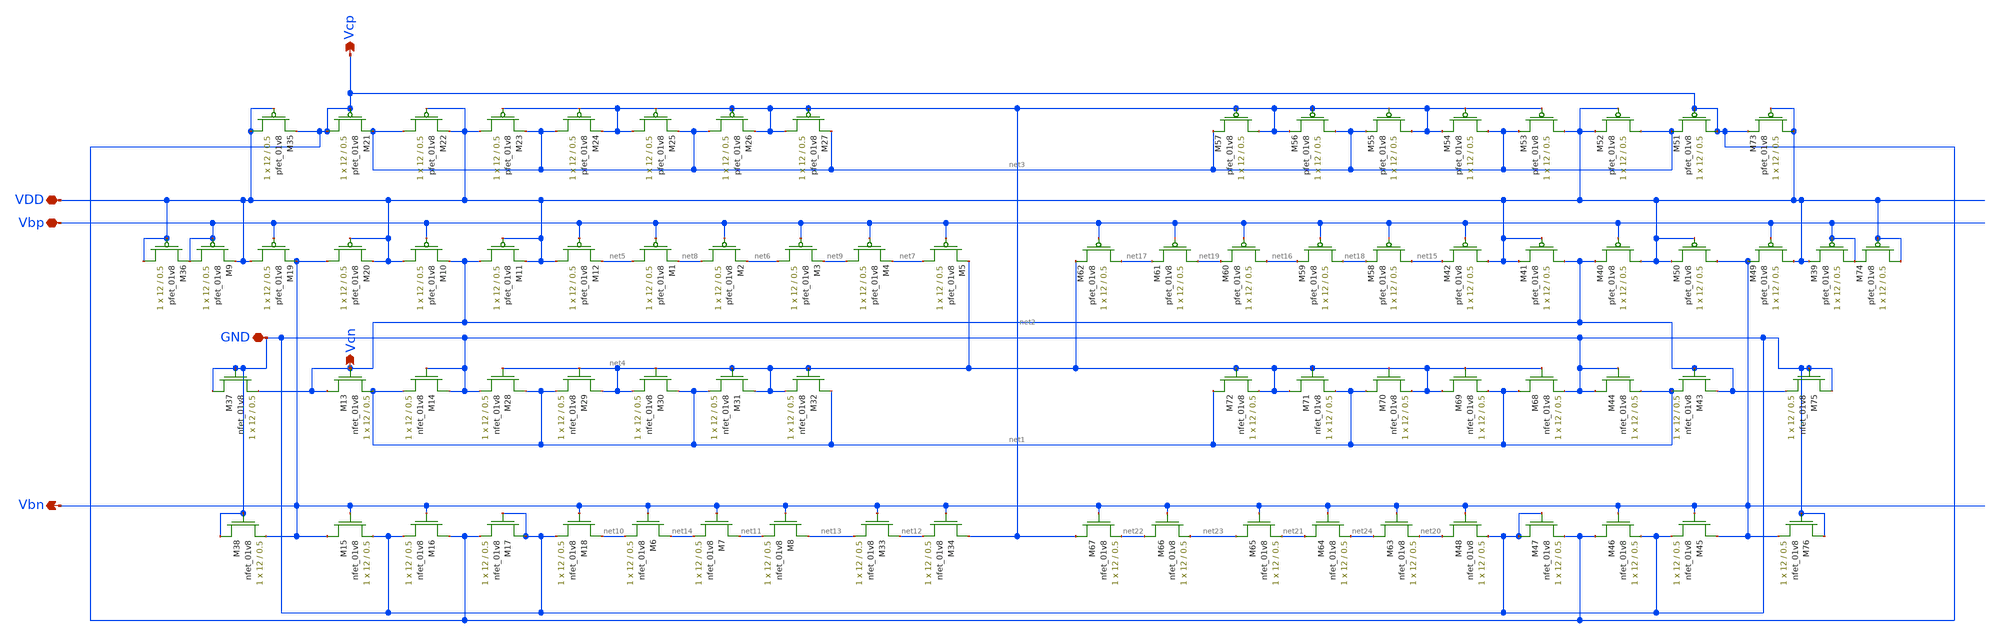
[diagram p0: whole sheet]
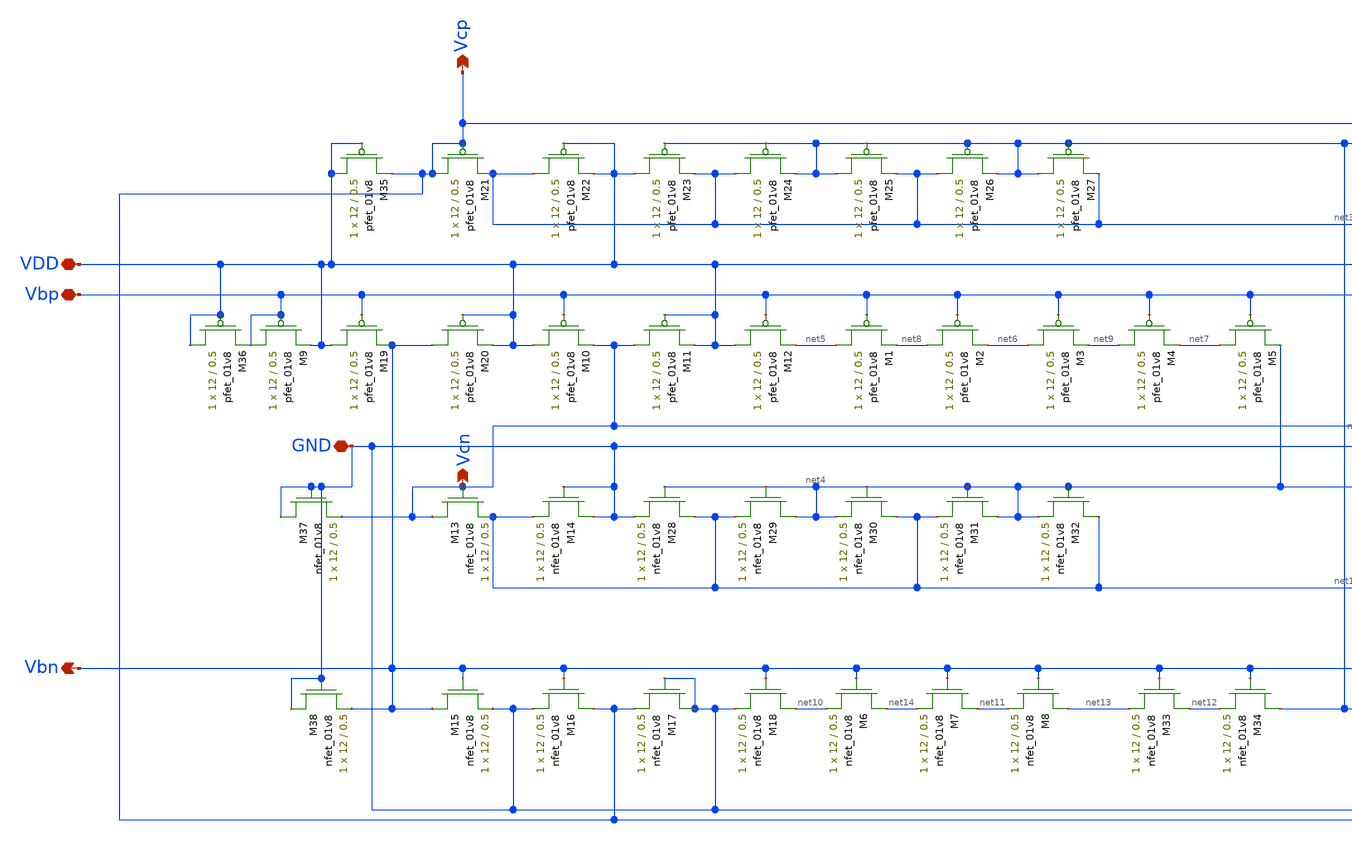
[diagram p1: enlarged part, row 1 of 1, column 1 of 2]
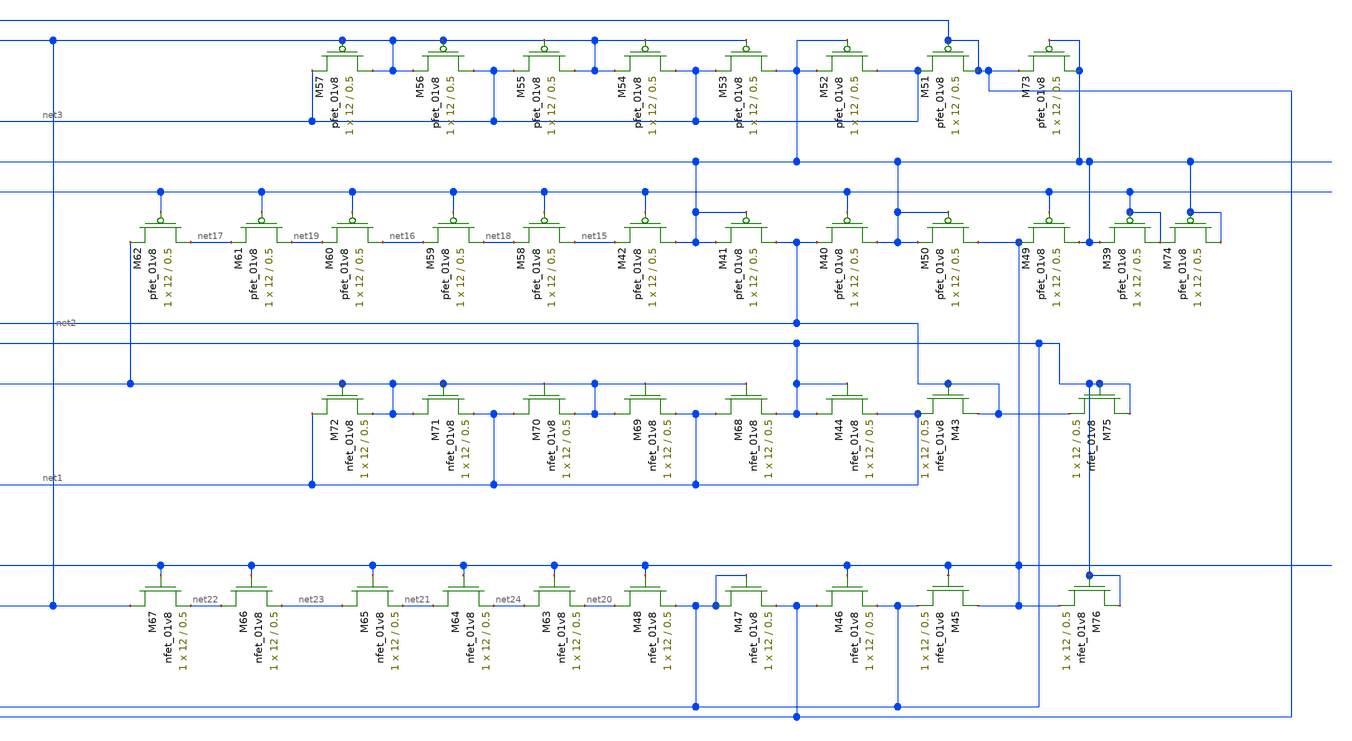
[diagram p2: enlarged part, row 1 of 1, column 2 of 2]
** sch_path: Miniproject3/Bias/LDS_Cascode_bias_voltage_generator.sch
**.subckt LDS_Cascode_bias_voltage_generator VDD Vbp Vcn GND Vbn Vcp
*.iopin VDD
*.iopin Vbp
*.opin Vcn
*.iopin GND
*.opin Vbn
*.opin Vcp
XM9 Vbp Vbp VDD VDD sky130_fd_pr__pfet_01v8 L=0.5 W=12 nf=1 ad='int((nf+1)/2) * W/nf * 0.29' as='int((nf+2)/2) * W/nf * 0.29'
+ pd='2*int((nf+1)/2) * (W/nf + 0.29)' ps='2*int((nf+2)/2) * (W/nf + 0.29)' nrd='0.29 / W' nrs='0.29 / W'
+ sa=0 sb=0 sd=0 mult=1 m=1
XM10 VDD Vbp Vcn VDD sky130_fd_pr__pfet_01v8 L=0.5 W=12 nf=1 ad='int((nf+1)/2) * W/nf * 0.29' as='int((nf+2)/2) * W/nf * 0.29'
+ pd='2*int((nf+1)/2) * (W/nf + 0.29)' ps='2*int((nf+2)/2) * (W/nf + 0.29)' nrd='0.29 / W' nrs='0.29 / W'
+ sa=0 sb=0 sd=0 mult=1 m=1
XM11 Vcn VDD VDD VDD sky130_fd_pr__pfet_01v8 L=0.5 W=12 nf=1 ad='int((nf+1)/2) * W/nf * 0.29' as='int((nf+2)/2) * W/nf * 0.29'
+ pd='2*int((nf+1)/2) * (W/nf + 0.29)' ps='2*int((nf+2)/2) * (W/nf + 0.29)' nrd='0.29 / W' nrs='0.29 / W'
+ sa=0 sb=0 sd=0 mult=1 m=1
XM12 VDD Vbp net5 VDD sky130_fd_pr__pfet_01v8 L=0.5 W=12 nf=1 ad='int((nf+1)/2) * W/nf * 0.29' as='int((nf+2)/2) * W/nf * 0.29'
+ pd='2*int((nf+1)/2) * (W/nf + 0.29)' ps='2*int((nf+2)/2) * (W/nf + 0.29)' nrd='0.29 / W' nrs='0.29 / W'
+ sa=0 sb=0 sd=0 mult=1 m=1
XM13 Vcn Vcn net1 GND sky130_fd_pr__nfet_01v8 L=0.5 W=12 nf=1 ad='int((nf+1)/2) * W/nf * 0.29' as='int((nf+2)/2) * W/nf * 0.29'
+ pd='2*int((nf+1)/2) * (W/nf + 0.29)' ps='2*int((nf+2)/2) * (W/nf + 0.29)' nrd='0.29 / W' nrs='0.29 / W'
+ sa=0 sb=0 sd=0 mult=1 m=1
XM14 GND GND net1 GND sky130_fd_pr__nfet_01v8 L=0.5 W=12 nf=1 ad='int((nf+1)/2) * W/nf * 0.29' as='int((nf+2)/2) * W/nf * 0.29'
+ pd='2*int((nf+1)/2) * (W/nf + 0.29)' ps='2*int((nf+2)/2) * (W/nf + 0.29)' nrd='0.29 / W' nrs='0.29 / W'
+ sa=0 sb=0 sd=0 mult=1 m=1
XM15 Vbn Vbn GND GND sky130_fd_pr__nfet_01v8 L=0.5 W=12 nf=1 ad='int((nf+1)/2) * W/nf * 0.29' as='int((nf+2)/2) * W/nf * 0.29'
+ pd='2*int((nf+1)/2) * (W/nf + 0.29)' ps='2*int((nf+2)/2) * (W/nf + 0.29)' nrd='0.29 / W' nrs='0.29 / W'
+ sa=0 sb=0 sd=0 mult=1 m=1
XM16 Vcp Vbn GND GND sky130_fd_pr__nfet_01v8 L=0.5 W=12 nf=1 ad='int((nf+1)/2) * W/nf * 0.29' as='int((nf+2)/2) * W/nf * 0.29'
+ pd='2*int((nf+1)/2) * (W/nf + 0.29)' ps='2*int((nf+2)/2) * (W/nf + 0.29)' nrd='0.29 / W' nrs='0.29 / W'
+ sa=0 sb=0 sd=0 mult=1 m=1
XM17 GND GND Vcp GND sky130_fd_pr__nfet_01v8 L=0.5 W=12 nf=1 ad='int((nf+1)/2) * W/nf * 0.29' as='int((nf+2)/2) * W/nf * 0.29'
+ pd='2*int((nf+1)/2) * (W/nf + 0.29)' ps='2*int((nf+2)/2) * (W/nf + 0.29)' nrd='0.29 / W' nrs='0.29 / W'
+ sa=0 sb=0 sd=0 mult=1 m=1
XM18 net10 Vbn GND GND sky130_fd_pr__nfet_01v8 L=0.5 W=12 nf=1 ad='int((nf+1)/2) * W/nf * 0.29' as='int((nf+2)/2) * W/nf * 0.29'
+ pd='2*int((nf+1)/2) * (W/nf + 0.29)' ps='2*int((nf+2)/2) * (W/nf + 0.29)' nrd='0.29 / W' nrs='0.29 / W'
+ sa=0 sb=0 sd=0 mult=1 m=1
XM19 VDD Vbp Vbn VDD sky130_fd_pr__pfet_01v8 L=0.5 W=12 nf=1 ad='int((nf+1)/2) * W/nf * 0.29' as='int((nf+2)/2) * W/nf * 0.29'
+ pd='2*int((nf+1)/2) * (W/nf + 0.29)' ps='2*int((nf+2)/2) * (W/nf + 0.29)' nrd='0.29 / W' nrs='0.29 / W'
+ sa=0 sb=0 sd=0 mult=1 m=1
XM20 Vbn VDD VDD VDD sky130_fd_pr__pfet_01v8 L=0.5 W=12 nf=1 ad='int((nf+1)/2) * W/nf * 0.29' as='int((nf+2)/2) * W/nf * 0.29'
+ pd='2*int((nf+1)/2) * (W/nf + 0.29)' ps='2*int((nf+2)/2) * (W/nf + 0.29)' nrd='0.29 / W' nrs='0.29 / W'
+ sa=0 sb=0 sd=0 mult=1 m=1
XM21 Vcp Vcp net3 VDD sky130_fd_pr__pfet_01v8 L=0.5 W=12 nf=1 ad='int((nf+1)/2) * W/nf * 0.29' as='int((nf+2)/2) * W/nf * 0.29'
+ pd='2*int((nf+1)/2) * (W/nf + 0.29)' ps='2*int((nf+2)/2) * (W/nf + 0.29)' nrd='0.29 / W' nrs='0.29 / W'
+ sa=0 sb=0 sd=0 mult=1 m=1
XM22 net3 VDD VDD VDD sky130_fd_pr__pfet_01v8 L=0.5 W=12 nf=1 ad='int((nf+1)/2) * W/nf * 0.29' as='int((nf+2)/2) * W/nf * 0.29'
+ pd='2*int((nf+1)/2) * (W/nf + 0.29)' ps='2*int((nf+2)/2) * (W/nf + 0.29)' nrd='0.29 / W' nrs='0.29 / W'
+ sa=0 sb=0 sd=0 mult=1 m=1
XM23 VDD net2 net3 VDD sky130_fd_pr__pfet_01v8 L=0.5 W=12 nf=1 ad='int((nf+1)/2) * W/nf * 0.29' as='int((nf+2)/2) * W/nf * 0.29'
+ pd='2*int((nf+1)/2) * (W/nf + 0.29)' ps='2*int((nf+2)/2) * (W/nf + 0.29)' nrd='0.29 / W' nrs='0.29 / W'
+ sa=0 sb=0 sd=0 mult=1 m=1
XM24 net3 net2 net2 VDD sky130_fd_pr__pfet_01v8 L=0.5 W=12 nf=1 ad='int((nf+1)/2) * W/nf * 0.29' as='int((nf+2)/2) * W/nf * 0.29'
+ pd='2*int((nf+1)/2) * (W/nf + 0.29)' ps='2*int((nf+2)/2) * (W/nf + 0.29)' nrd='0.29 / W' nrs='0.29 / W'
+ sa=0 sb=0 sd=0 mult=1 m=1
XM25 net2 net2 net3 VDD sky130_fd_pr__pfet_01v8 L=0.5 W=12 nf=1 ad='int((nf+1)/2) * W/nf * 0.29' as='int((nf+2)/2) * W/nf * 0.29'
+ pd='2*int((nf+1)/2) * (W/nf + 0.29)' ps='2*int((nf+2)/2) * (W/nf + 0.29)' nrd='0.29 / W' nrs='0.29 / W'
+ sa=0 sb=0 sd=0 mult=1 m=1
XM26 net3 net2 net2 VDD sky130_fd_pr__pfet_01v8 L=0.5 W=12 nf=1 ad='int((nf+1)/2) * W/nf * 0.29' as='int((nf+2)/2) * W/nf * 0.29'
+ pd='2*int((nf+1)/2) * (W/nf + 0.29)' ps='2*int((nf+2)/2) * (W/nf + 0.29)' nrd='0.29 / W' nrs='0.29 / W'
+ sa=0 sb=0 sd=0 mult=1 m=1
XM27 net2 net2 net3 VDD sky130_fd_pr__pfet_01v8 L=0.5 W=12 nf=1 ad='int((nf+1)/2) * W/nf * 0.29' as='int((nf+2)/2) * W/nf * 0.29'
+ pd='2*int((nf+1)/2) * (W/nf + 0.29)' ps='2*int((nf+2)/2) * (W/nf + 0.29)' nrd='0.29 / W' nrs='0.29 / W'
+ sa=0 sb=0 sd=0 mult=1 m=1
XM1 net5 Vbp net8 VDD sky130_fd_pr__pfet_01v8 L=0.5 W=12 nf=1 ad='int((nf+1)/2) * W/nf * 0.29' as='int((nf+2)/2) * W/nf * 0.29'
+ pd='2*int((nf+1)/2) * (W/nf + 0.29)' ps='2*int((nf+2)/2) * (W/nf + 0.29)' nrd='0.29 / W' nrs='0.29 / W'
+ sa=0 sb=0 sd=0 mult=1 m=1
XM2 net8 Vbp net6 VDD sky130_fd_pr__pfet_01v8 L=0.5 W=12 nf=1 ad='int((nf+1)/2) * W/nf * 0.29' as='int((nf+2)/2) * W/nf * 0.29'
+ pd='2*int((nf+1)/2) * (W/nf + 0.29)' ps='2*int((nf+2)/2) * (W/nf + 0.29)' nrd='0.29 / W' nrs='0.29 / W'
+ sa=0 sb=0 sd=0 mult=1 m=1
XM3 net6 Vbp net9 VDD sky130_fd_pr__pfet_01v8 L=0.5 W=12 nf=1 ad='int((nf+1)/2) * W/nf * 0.29' as='int((nf+2)/2) * W/nf * 0.29'
+ pd='2*int((nf+1)/2) * (W/nf + 0.29)' ps='2*int((nf+2)/2) * (W/nf + 0.29)' nrd='0.29 / W' nrs='0.29 / W'
+ sa=0 sb=0 sd=0 mult=1 m=1
XM4 net9 Vbp net7 VDD sky130_fd_pr__pfet_01v8 L=0.5 W=12 nf=1 ad='int((nf+1)/2) * W/nf * 0.29' as='int((nf+2)/2) * W/nf * 0.29'
+ pd='2*int((nf+1)/2) * (W/nf + 0.29)' ps='2*int((nf+2)/2) * (W/nf + 0.29)' nrd='0.29 / W' nrs='0.29 / W'
+ sa=0 sb=0 sd=0 mult=1 m=1
XM5 net7 Vbp net4 VDD sky130_fd_pr__pfet_01v8 L=0.5 W=12 nf=1 ad='int((nf+1)/2) * W/nf * 0.29' as='int((nf+2)/2) * W/nf * 0.29'
+ pd='2*int((nf+1)/2) * (W/nf + 0.29)' ps='2*int((nf+2)/2) * (W/nf + 0.29)' nrd='0.29 / W' nrs='0.29 / W'
+ sa=0 sb=0 sd=0 mult=1 m=1
XM6 net14 Vbn net10 GND sky130_fd_pr__nfet_01v8 L=0.5 W=12 nf=1 ad='int((nf+1)/2) * W/nf * 0.29' as='int((nf+2)/2) * W/nf * 0.29'
+ pd='2*int((nf+1)/2) * (W/nf + 0.29)' ps='2*int((nf+2)/2) * (W/nf + 0.29)' nrd='0.29 / W' nrs='0.29 / W'
+ sa=0 sb=0 sd=0 mult=1 m=1
XM7 net11 Vbn net14 GND sky130_fd_pr__nfet_01v8 L=0.5 W=12 nf=1 ad='int((nf+1)/2) * W/nf * 0.29' as='int((nf+2)/2) * W/nf * 0.29'
+ pd='2*int((nf+1)/2) * (W/nf + 0.29)' ps='2*int((nf+2)/2) * (W/nf + 0.29)' nrd='0.29 / W' nrs='0.29 / W'
+ sa=0 sb=0 sd=0 mult=1 m=1
XM8 net13 Vbn net11 GND sky130_fd_pr__nfet_01v8 L=0.5 W=12 nf=1 ad='int((nf+1)/2) * W/nf * 0.29' as='int((nf+2)/2) * W/nf * 0.29'
+ pd='2*int((nf+1)/2) * (W/nf + 0.29)' ps='2*int((nf+2)/2) * (W/nf + 0.29)' nrd='0.29 / W' nrs='0.29 / W'
+ sa=0 sb=0 sd=0 mult=1 m=1
XM33 net12 Vbn net13 GND sky130_fd_pr__nfet_01v8 L=0.5 W=12 nf=1 ad='int((nf+1)/2) * W/nf * 0.29' as='int((nf+2)/2) * W/nf * 0.29'
+ pd='2*int((nf+1)/2) * (W/nf + 0.29)' ps='2*int((nf+2)/2) * (W/nf + 0.29)' nrd='0.29 / W' nrs='0.29 / W'
+ sa=0 sb=0 sd=0 mult=1 m=1
XM34 net2 Vbn net12 GND sky130_fd_pr__nfet_01v8 L=0.5 W=12 nf=1 ad='int((nf+1)/2) * W/nf * 0.29' as='int((nf+2)/2) * W/nf * 0.29'
+ pd='2*int((nf+1)/2) * (W/nf + 0.29)' ps='2*int((nf+2)/2) * (W/nf + 0.29)' nrd='0.29 / W' nrs='0.29 / W'
+ sa=0 sb=0 sd=0 mult=1 m=1
XM28 net1 net4 GND GND sky130_fd_pr__nfet_01v8 L=0.5 W=12 nf=1 ad='int((nf+1)/2) * W/nf * 0.29' as='int((nf+2)/2) * W/nf * 0.29'
+ pd='2*int((nf+1)/2) * (W/nf + 0.29)' ps='2*int((nf+2)/2) * (W/nf + 0.29)' nrd='0.29 / W' nrs='0.29 / W'
+ sa=0 sb=0 sd=0 mult=1 m=1
XM29 net4 net4 net1 GND sky130_fd_pr__nfet_01v8 L=0.5 W=12 nf=1 ad='int((nf+1)/2) * W/nf * 0.29' as='int((nf+2)/2) * W/nf * 0.29'
+ pd='2*int((nf+1)/2) * (W/nf + 0.29)' ps='2*int((nf+2)/2) * (W/nf + 0.29)' nrd='0.29 / W' nrs='0.29 / W'
+ sa=0 sb=0 sd=0 mult=1 m=1
XM30 net1 net4 net4 GND sky130_fd_pr__nfet_01v8 L=0.5 W=12 nf=1 ad='int((nf+1)/2) * W/nf * 0.29' as='int((nf+2)/2) * W/nf * 0.29'
+ pd='2*int((nf+1)/2) * (W/nf + 0.29)' ps='2*int((nf+2)/2) * (W/nf + 0.29)' nrd='0.29 / W' nrs='0.29 / W'
+ sa=0 sb=0 sd=0 mult=1 m=1
XM31 net4 net4 net1 GND sky130_fd_pr__nfet_01v8 L=0.5 W=12 nf=1 ad='int((nf+1)/2) * W/nf * 0.29' as='int((nf+2)/2) * W/nf * 0.29'
+ pd='2*int((nf+1)/2) * (W/nf + 0.29)' ps='2*int((nf+2)/2) * (W/nf + 0.29)' nrd='0.29 / W' nrs='0.29 / W'
+ sa=0 sb=0 sd=0 mult=1 m=1
XM32 net1 net4 net4 GND sky130_fd_pr__nfet_01v8 L=0.5 W=12 nf=1 ad='int((nf+1)/2) * W/nf * 0.29' as='int((nf+2)/2) * W/nf * 0.29'
+ pd='2*int((nf+1)/2) * (W/nf + 0.29)' ps='2*int((nf+2)/2) * (W/nf + 0.29)' nrd='0.29 / W' nrs='0.29 / W'
+ sa=0 sb=0 sd=0 mult=1 m=1
XM35 VDD VDD Vcp VDD sky130_fd_pr__pfet_01v8 L=0.5 W=12 nf=1 ad='int((nf+1)/2) * W/nf * 0.29' as='int((nf+2)/2) * W/nf * 0.29'
+ pd='2*int((nf+1)/2) * (W/nf + 0.29)' ps='2*int((nf+2)/2) * (W/nf + 0.29)' nrd='0.29 / W' nrs='0.29 / W'
+ sa=0 sb=0 sd=0 mult=1 m=1
XM36 VDD VDD Vbp VDD sky130_fd_pr__pfet_01v8 L=0.5 W=12 nf=1 ad='int((nf+1)/2) * W/nf * 0.29' as='int((nf+2)/2) * W/nf * 0.29'
+ pd='2*int((nf+1)/2) * (W/nf + 0.29)' ps='2*int((nf+2)/2) * (W/nf + 0.29)' nrd='0.29 / W' nrs='0.29 / W'
+ sa=0 sb=0 sd=0 mult=1 m=1
XM37 GND GND Vcn GND sky130_fd_pr__nfet_01v8 L=0.5 W=12 nf=1 ad='int((nf+1)/2) * W/nf * 0.29' as='int((nf+2)/2) * W/nf * 0.29'
+ pd='2*int((nf+1)/2) * (W/nf + 0.29)' ps='2*int((nf+2)/2) * (W/nf + 0.29)' nrd='0.29 / W' nrs='0.29 / W'
+ sa=0 sb=0 sd=0 mult=1 m=1
XM38 GND GND Vbn GND sky130_fd_pr__nfet_01v8 L=0.5 W=12 nf=1 ad='int((nf+1)/2) * W/nf * 0.29' as='int((nf+2)/2) * W/nf * 0.29'
+ pd='2*int((nf+1)/2) * (W/nf + 0.29)' ps='2*int((nf+2)/2) * (W/nf + 0.29)' nrd='0.29 / W' nrs='0.29 / W'
+ sa=0 sb=0 sd=0 mult=1 m=1
XM39 Vbp Vbp VDD VDD sky130_fd_pr__pfet_01v8 L=0.5 W=12 nf=1 ad='int((nf+1)/2) * W/nf * 0.29' as='int((nf+2)/2) * W/nf * 0.29'
+ pd='2*int((nf+1)/2) * (W/nf + 0.29)' ps='2*int((nf+2)/2) * (W/nf + 0.29)' nrd='0.29 / W' nrs='0.29 / W'
+ sa=0 sb=0 sd=0 mult=1 m=1
XM40 VDD Vbp Vcn VDD sky130_fd_pr__pfet_01v8 L=0.5 W=12 nf=1 ad='int((nf+1)/2) * W/nf * 0.29' as='int((nf+2)/2) * W/nf * 0.29'
+ pd='2*int((nf+1)/2) * (W/nf + 0.29)' ps='2*int((nf+2)/2) * (W/nf + 0.29)' nrd='0.29 / W' nrs='0.29 / W'
+ sa=0 sb=0 sd=0 mult=1 m=1
XM41 Vcn VDD VDD VDD sky130_fd_pr__pfet_01v8 L=0.5 W=12 nf=1 ad='int((nf+1)/2) * W/nf * 0.29' as='int((nf+2)/2) * W/nf * 0.29'
+ pd='2*int((nf+1)/2) * (W/nf + 0.29)' ps='2*int((nf+2)/2) * (W/nf + 0.29)' nrd='0.29 / W' nrs='0.29 / W'
+ sa=0 sb=0 sd=0 mult=1 m=1
XM42 VDD Vbp net15 VDD sky130_fd_pr__pfet_01v8 L=0.5 W=12 nf=1 ad='int((nf+1)/2) * W/nf * 0.29' as='int((nf+2)/2) * W/nf * 0.29'
+ pd='2*int((nf+1)/2) * (W/nf + 0.29)' ps='2*int((nf+2)/2) * (W/nf + 0.29)' nrd='0.29 / W' nrs='0.29 / W'
+ sa=0 sb=0 sd=0 mult=1 m=1
XM43 Vcn Vcn net1 GND sky130_fd_pr__nfet_01v8 L=0.5 W=12 nf=1 ad='int((nf+1)/2) * W/nf * 0.29' as='int((nf+2)/2) * W/nf * 0.29'
+ pd='2*int((nf+1)/2) * (W/nf + 0.29)' ps='2*int((nf+2)/2) * (W/nf + 0.29)' nrd='0.29 / W' nrs='0.29 / W'
+ sa=0 sb=0 sd=0 mult=1 m=1
XM44 GND GND net1 GND sky130_fd_pr__nfet_01v8 L=0.5 W=12 nf=1 ad='int((nf+1)/2) * W/nf * 0.29' as='int((nf+2)/2) * W/nf * 0.29'
+ pd='2*int((nf+1)/2) * (W/nf + 0.29)' ps='2*int((nf+2)/2) * (W/nf + 0.29)' nrd='0.29 / W' nrs='0.29 / W'
+ sa=0 sb=0 sd=0 mult=1 m=1
XM45 Vbn Vbn GND GND sky130_fd_pr__nfet_01v8 L=0.5 W=12 nf=1 ad='int((nf+1)/2) * W/nf * 0.29' as='int((nf+2)/2) * W/nf * 0.29'
+ pd='2*int((nf+1)/2) * (W/nf + 0.29)' ps='2*int((nf+2)/2) * (W/nf + 0.29)' nrd='0.29 / W' nrs='0.29 / W'
+ sa=0 sb=0 sd=0 mult=1 m=1
XM46 Vcp Vbn GND GND sky130_fd_pr__nfet_01v8 L=0.5 W=12 nf=1 ad='int((nf+1)/2) * W/nf * 0.29' as='int((nf+2)/2) * W/nf * 0.29'
+ pd='2*int((nf+1)/2) * (W/nf + 0.29)' ps='2*int((nf+2)/2) * (W/nf + 0.29)' nrd='0.29 / W' nrs='0.29 / W'
+ sa=0 sb=0 sd=0 mult=1 m=1
XM47 GND GND Vcp GND sky130_fd_pr__nfet_01v8 L=0.5 W=12 nf=1 ad='int((nf+1)/2) * W/nf * 0.29' as='int((nf+2)/2) * W/nf * 0.29'
+ pd='2*int((nf+1)/2) * (W/nf + 0.29)' ps='2*int((nf+2)/2) * (W/nf + 0.29)' nrd='0.29 / W' nrs='0.29 / W'
+ sa=0 sb=0 sd=0 mult=1 m=1
XM48 net20 Vbn GND GND sky130_fd_pr__nfet_01v8 L=0.5 W=12 nf=1 ad='int((nf+1)/2) * W/nf * 0.29' as='int((nf+2)/2) * W/nf * 0.29'
+ pd='2*int((nf+1)/2) * (W/nf + 0.29)' ps='2*int((nf+2)/2) * (W/nf + 0.29)' nrd='0.29 / W' nrs='0.29 / W'
+ sa=0 sb=0 sd=0 mult=1 m=1
XM49 VDD Vbp Vbn VDD sky130_fd_pr__pfet_01v8 L=0.5 W=12 nf=1 ad='int((nf+1)/2) * W/nf * 0.29' as='int((nf+2)/2) * W/nf * 0.29'
+ pd='2*int((nf+1)/2) * (W/nf + 0.29)' ps='2*int((nf+2)/2) * (W/nf + 0.29)' nrd='0.29 / W' nrs='0.29 / W'
+ sa=0 sb=0 sd=0 mult=1 m=1
XM50 Vbn VDD VDD VDD sky130_fd_pr__pfet_01v8 L=0.5 W=12 nf=1 ad='int((nf+1)/2) * W/nf * 0.29' as='int((nf+2)/2) * W/nf * 0.29'
+ pd='2*int((nf+1)/2) * (W/nf + 0.29)' ps='2*int((nf+2)/2) * (W/nf + 0.29)' nrd='0.29 / W' nrs='0.29 / W'
+ sa=0 sb=0 sd=0 mult=1 m=1
XM51 Vcp Vcp net3 VDD sky130_fd_pr__pfet_01v8 L=0.5 W=12 nf=1 ad='int((nf+1)/2) * W/nf * 0.29' as='int((nf+2)/2) * W/nf * 0.29'
+ pd='2*int((nf+1)/2) * (W/nf + 0.29)' ps='2*int((nf+2)/2) * (W/nf + 0.29)' nrd='0.29 / W' nrs='0.29 / W'
+ sa=0 sb=0 sd=0 mult=1 m=1
XM52 net3 VDD VDD VDD sky130_fd_pr__pfet_01v8 L=0.5 W=12 nf=1 ad='int((nf+1)/2) * W/nf * 0.29' as='int((nf+2)/2) * W/nf * 0.29'
+ pd='2*int((nf+1)/2) * (W/nf + 0.29)' ps='2*int((nf+2)/2) * (W/nf + 0.29)' nrd='0.29 / W' nrs='0.29 / W'
+ sa=0 sb=0 sd=0 mult=1 m=1
XM53 VDD net2 net3 VDD sky130_fd_pr__pfet_01v8 L=0.5 W=12 nf=1 ad='int((nf+1)/2) * W/nf * 0.29' as='int((nf+2)/2) * W/nf * 0.29'
+ pd='2*int((nf+1)/2) * (W/nf + 0.29)' ps='2*int((nf+2)/2) * (W/nf + 0.29)' nrd='0.29 / W' nrs='0.29 / W'
+ sa=0 sb=0 sd=0 mult=1 m=1
XM54 net3 net2 net2 VDD sky130_fd_pr__pfet_01v8 L=0.5 W=12 nf=1 ad='int((nf+1)/2) * W/nf * 0.29' as='int((nf+2)/2) * W/nf * 0.29'
+ pd='2*int((nf+1)/2) * (W/nf + 0.29)' ps='2*int((nf+2)/2) * (W/nf + 0.29)' nrd='0.29 / W' nrs='0.29 / W'
+ sa=0 sb=0 sd=0 mult=1 m=1
XM55 net2 net2 net3 VDD sky130_fd_pr__pfet_01v8 L=0.5 W=12 nf=1 ad='int((nf+1)/2) * W/nf * 0.29' as='int((nf+2)/2) * W/nf * 0.29'
+ pd='2*int((nf+1)/2) * (W/nf + 0.29)' ps='2*int((nf+2)/2) * (W/nf + 0.29)' nrd='0.29 / W' nrs='0.29 / W'
+ sa=0 sb=0 sd=0 mult=1 m=1
XM56 net3 net2 net2 VDD sky130_fd_pr__pfet_01v8 L=0.5 W=12 nf=1 ad='int((nf+1)/2) * W/nf * 0.29' as='int((nf+2)/2) * W/nf * 0.29'
+ pd='2*int((nf+1)/2) * (W/nf + 0.29)' ps='2*int((nf+2)/2) * (W/nf + 0.29)' nrd='0.29 / W' nrs='0.29 / W'
+ sa=0 sb=0 sd=0 mult=1 m=1
XM57 net2 net2 net3 VDD sky130_fd_pr__pfet_01v8 L=0.5 W=12 nf=1 ad='int((nf+1)/2) * W/nf * 0.29' as='int((nf+2)/2) * W/nf * 0.29'
+ pd='2*int((nf+1)/2) * (W/nf + 0.29)' ps='2*int((nf+2)/2) * (W/nf + 0.29)' nrd='0.29 / W' nrs='0.29 / W'
+ sa=0 sb=0 sd=0 mult=1 m=1
XM58 net15 Vbp net18 VDD sky130_fd_pr__pfet_01v8 L=0.5 W=12 nf=1 ad='int((nf+1)/2) * W/nf * 0.29' as='int((nf+2)/2) * W/nf * 0.29'
+ pd='2*int((nf+1)/2) * (W/nf + 0.29)' ps='2*int((nf+2)/2) * (W/nf + 0.29)' nrd='0.29 / W' nrs='0.29 / W'
+ sa=0 sb=0 sd=0 mult=1 m=1
XM59 net18 Vbp net16 VDD sky130_fd_pr__pfet_01v8 L=0.5 W=12 nf=1 ad='int((nf+1)/2) * W/nf * 0.29' as='int((nf+2)/2) * W/nf * 0.29'
+ pd='2*int((nf+1)/2) * (W/nf + 0.29)' ps='2*int((nf+2)/2) * (W/nf + 0.29)' nrd='0.29 / W' nrs='0.29 / W'
+ sa=0 sb=0 sd=0 mult=1 m=1
XM60 net16 Vbp net19 VDD sky130_fd_pr__pfet_01v8 L=0.5 W=12 nf=1 ad='int((nf+1)/2) * W/nf * 0.29' as='int((nf+2)/2) * W/nf * 0.29'
+ pd='2*int((nf+1)/2) * (W/nf + 0.29)' ps='2*int((nf+2)/2) * (W/nf + 0.29)' nrd='0.29 / W' nrs='0.29 / W'
+ sa=0 sb=0 sd=0 mult=1 m=1
XM61 net19 Vbp net17 VDD sky130_fd_pr__pfet_01v8 L=0.5 W=12 nf=1 ad='int((nf+1)/2) * W/nf * 0.29' as='int((nf+2)/2) * W/nf * 0.29'
+ pd='2*int((nf+1)/2) * (W/nf + 0.29)' ps='2*int((nf+2)/2) * (W/nf + 0.29)' nrd='0.29 / W' nrs='0.29 / W'
+ sa=0 sb=0 sd=0 mult=1 m=1
XM62 net17 Vbp net4 VDD sky130_fd_pr__pfet_01v8 L=0.5 W=12 nf=1 ad='int((nf+1)/2) * W/nf * 0.29' as='int((nf+2)/2) * W/nf * 0.29'
+ pd='2*int((nf+1)/2) * (W/nf + 0.29)' ps='2*int((nf+2)/2) * (W/nf + 0.29)' nrd='0.29 / W' nrs='0.29 / W'
+ sa=0 sb=0 sd=0 mult=1 m=1
XM63 net24 Vbn net20 GND sky130_fd_pr__nfet_01v8 L=0.5 W=12 nf=1 ad='int((nf+1)/2) * W/nf * 0.29' as='int((nf+2)/2) * W/nf * 0.29'
+ pd='2*int((nf+1)/2) * (W/nf + 0.29)' ps='2*int((nf+2)/2) * (W/nf + 0.29)' nrd='0.29 / W' nrs='0.29 / W'
+ sa=0 sb=0 sd=0 mult=1 m=1
XM64 net21 Vbn net24 GND sky130_fd_pr__nfet_01v8 L=0.5 W=12 nf=1 ad='int((nf+1)/2) * W/nf * 0.29' as='int((nf+2)/2) * W/nf * 0.29'
+ pd='2*int((nf+1)/2) * (W/nf + 0.29)' ps='2*int((nf+2)/2) * (W/nf + 0.29)' nrd='0.29 / W' nrs='0.29 / W'
+ sa=0 sb=0 sd=0 mult=1 m=1
XM65 net23 Vbn net21 GND sky130_fd_pr__nfet_01v8 L=0.5 W=12 nf=1 ad='int((nf+1)/2) * W/nf * 0.29' as='int((nf+2)/2) * W/nf * 0.29'
+ pd='2*int((nf+1)/2) * (W/nf + 0.29)' ps='2*int((nf+2)/2) * (W/nf + 0.29)' nrd='0.29 / W' nrs='0.29 / W'
+ sa=0 sb=0 sd=0 mult=1 m=1
XM66 net22 Vbn net23 GND sky130_fd_pr__nfet_01v8 L=0.5 W=12 nf=1 ad='int((nf+1)/2) * W/nf * 0.29' as='int((nf+2)/2) * W/nf * 0.29'
+ pd='2*int((nf+1)/2) * (W/nf + 0.29)' ps='2*int((nf+2)/2) * (W/nf + 0.29)' nrd='0.29 / W' nrs='0.29 / W'
+ sa=0 sb=0 sd=0 mult=1 m=1
XM67 net2 Vbn net22 GND sky130_fd_pr__nfet_01v8 L=0.5 W=12 nf=1 ad='int((nf+1)/2) * W/nf * 0.29' as='int((nf+2)/2) * W/nf * 0.29'
+ pd='2*int((nf+1)/2) * (W/nf + 0.29)' ps='2*int((nf+2)/2) * (W/nf + 0.29)' nrd='0.29 / W' nrs='0.29 / W'
+ sa=0 sb=0 sd=0 mult=1 m=1
XM68 net1 net4 GND GND sky130_fd_pr__nfet_01v8 L=0.5 W=12 nf=1 ad='int((nf+1)/2) * W/nf * 0.29' as='int((nf+2)/2) * W/nf * 0.29'
+ pd='2*int((nf+1)/2) * (W/nf + 0.29)' ps='2*int((nf+2)/2) * (W/nf + 0.29)' nrd='0.29 / W' nrs='0.29 / W'
+ sa=0 sb=0 sd=0 mult=1 m=1
XM69 net4 net4 net1 GND sky130_fd_pr__nfet_01v8 L=0.5 W=12 nf=1 ad='int((nf+1)/2) * W/nf * 0.29' as='int((nf+2)/2) * W/nf * 0.29'
+ pd='2*int((nf+1)/2) * (W/nf + 0.29)' ps='2*int((nf+2)/2) * (W/nf + 0.29)' nrd='0.29 / W' nrs='0.29 / W'
+ sa=0 sb=0 sd=0 mult=1 m=1
XM70 net1 net4 net4 GND sky130_fd_pr__nfet_01v8 L=0.5 W=12 nf=1 ad='int((nf+1)/2) * W/nf * 0.29' as='int((nf+2)/2) * W/nf * 0.29'
+ pd='2*int((nf+1)/2) * (W/nf + 0.29)' ps='2*int((nf+2)/2) * (W/nf + 0.29)' nrd='0.29 / W' nrs='0.29 / W'
+ sa=0 sb=0 sd=0 mult=1 m=1
XM71 net4 net4 net1 GND sky130_fd_pr__nfet_01v8 L=0.5 W=12 nf=1 ad='int((nf+1)/2) * W/nf * 0.29' as='int((nf+2)/2) * W/nf * 0.29'
+ pd='2*int((nf+1)/2) * (W/nf + 0.29)' ps='2*int((nf+2)/2) * (W/nf + 0.29)' nrd='0.29 / W' nrs='0.29 / W'
+ sa=0 sb=0 sd=0 mult=1 m=1
XM72 net1 net4 net4 GND sky130_fd_pr__nfet_01v8 L=0.5 W=12 nf=1 ad='int((nf+1)/2) * W/nf * 0.29' as='int((nf+2)/2) * W/nf * 0.29'
+ pd='2*int((nf+1)/2) * (W/nf + 0.29)' ps='2*int((nf+2)/2) * (W/nf + 0.29)' nrd='0.29 / W' nrs='0.29 / W'
+ sa=0 sb=0 sd=0 mult=1 m=1
XM73 VDD VDD Vcp VDD sky130_fd_pr__pfet_01v8 L=0.5 W=12 nf=1 ad='int((nf+1)/2) * W/nf * 0.29' as='int((nf+2)/2) * W/nf * 0.29'
+ pd='2*int((nf+1)/2) * (W/nf + 0.29)' ps='2*int((nf+2)/2) * (W/nf + 0.29)' nrd='0.29 / W' nrs='0.29 / W'
+ sa=0 sb=0 sd=0 mult=1 m=1
XM74 VDD VDD Vbp VDD sky130_fd_pr__pfet_01v8 L=0.5 W=12 nf=1 ad='int((nf+1)/2) * W/nf * 0.29' as='int((nf+2)/2) * W/nf * 0.29'
+ pd='2*int((nf+1)/2) * (W/nf + 0.29)' ps='2*int((nf+2)/2) * (W/nf + 0.29)' nrd='0.29 / W' nrs='0.29 / W'
+ sa=0 sb=0 sd=0 mult=1 m=1
XM75 GND GND Vcn GND sky130_fd_pr__nfet_01v8 L=0.5 W=12 nf=1 ad='int((nf+1)/2) * W/nf * 0.29' as='int((nf+2)/2) * W/nf * 0.29'
+ pd='2*int((nf+1)/2) * (W/nf + 0.29)' ps='2*int((nf+2)/2) * (W/nf + 0.29)' nrd='0.29 / W' nrs='0.29 / W'
+ sa=0 sb=0 sd=0 mult=1 m=1
XM76 GND GND Vbn GND sky130_fd_pr__nfet_01v8 L=0.5 W=12 nf=1 ad='int((nf+1)/2) * W/nf * 0.29' as='int((nf+2)/2) * W/nf * 0.29'
+ pd='2*int((nf+1)/2) * (W/nf + 0.29)' ps='2*int((nf+2)/2) * (W/nf + 0.29)' nrd='0.29 / W' nrs='0.29 / W'
+ sa=0 sb=0 sd=0 mult=1 m=1
**.ends
.end
